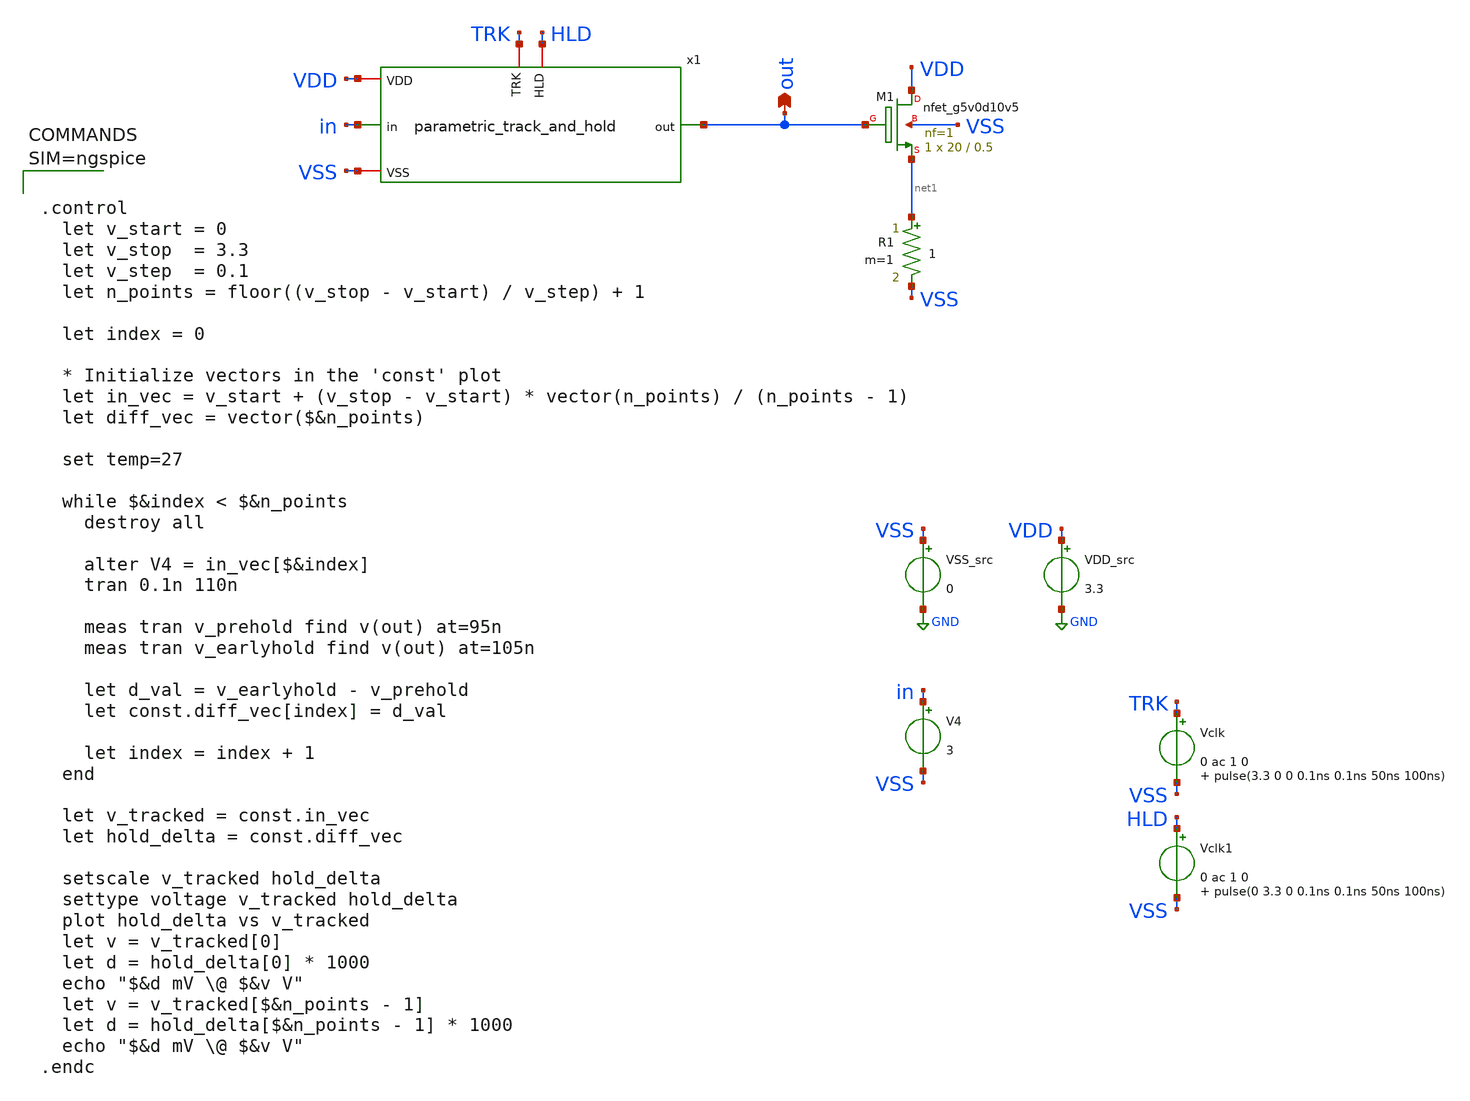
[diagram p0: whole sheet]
** sch_path: xschem/hold_testbench.sch
**.subckt hold_testbench out
*.opin out
VDD_src VDD GND 3.3
VSS_src VSS GND 0
V4 in VSS 3
XM1 VDD out net1 VSS sky130_fd_pr__nfet_g5v0d10v5 L=0.5 W=20 nf=1 ad='int((nf+1)/2) * W/nf * 0.29' as='int((nf+2)/2) * W/nf * 0.29'
+ pd='2*int((nf+1)/2) * (W/nf + 0.29)' ps='2*int((nf+2)/2) * (W/nf + 0.29)' nrd='0.29 / W' nrs='0.29 / W'
+ sa=0 sb=0 sd=0 mult=1 m=1
R1 net1 VSS 1 m=1
Vclk TRK VSS 0 ac 1 0 pulse(3.3 0 0 0.1ns 0.1ns 50ns 100ns)
Vclk1 HLD VSS 0 ac 1 0 pulse(0 3.3 0 0.1ns 0.1ns 50ns 100ns)
x1 HLD TRK VDD VSS out in parametric_track_and_hold WT=1 PFT=1.21 PF=2 WS=5 WB=5 CB=18
**** begin user architecture code

** opencircuitdesign pdks install
.lib $::SKYWATER_MODELS/sky130.lib.spice ss





.control
  let v_start = 0
  let v_stop  = 3.3
  let v_step  = 0.1
  let n_points = floor((v_stop - v_start) / v_step) + 1

  let index = 0

  * Initialize vectors in the 'const' plot
  let in_vec = v_start + (v_stop - v_start) * vector(n_points) / (n_points - 1)
  let diff_vec = vector($&n_points)

  set temp=27

  while $&index < $&n_points
    destroy all

    alter V4 = in_vec[$&index]
    tran 0.1n 110n

    meas tran v_prehold find v(out) at=95n
    meas tran v_earlyhold find v(out) at=105n

    let d_val = v_earlyhold - v_prehold
    let const.diff_vec[index] = d_val

    let index = index + 1
  end

  let v_tracked = const.in_vec
  let hold_delta = const.diff_vec

  setscale v_tracked hold_delta
  settype voltage v_tracked hold_delta
  plot hold_delta vs v_tracked
  let v = v_tracked[0]
  let d = hold_delta[0] * 1000
  echo "$&d mV \@ $&v V"
  let v = v_tracked[$&n_points - 1]
  let d = hold_delta[$&n_points - 1] * 1000
  echo "$&d mV \@ $&v V"
.endc



**** end user architecture code
**.ends

* expanding   symbol:  parametric_track_and_hold.sym # of pins=6
** sym_path: xschem/parametric_track_and_hold.sym
** sch_path: xschem/parametric_track_and_hold.sch
.subckt parametric_track_and_hold HLD TRK VDD VSS out in  WT=1 PFT=1.21 PF=2 WS=5 WB=5 CB=18
*.iopin VSS
*.iopin VDD
*.ipin in
*.opin out
*.iopin TRK
*.iopin HLD
XC1 out VSS sky130_fd_pr__cap_mim_m3_1 W=5 L=5 MF=1 m=1
XM1 out X in VSS sky130_fd_pr__nfet_g5v0d10v5 L=0.5 W={WT} nf=1 ad='int((nf+1)/2) * W/nf * 0.29' as='int((nf+2)/2) * W/nf * 0.29'
+ pd='2*int((nf+1)/2) * (W/nf + 0.29)' ps='2*int((nf+2)/2) * (W/nf + 0.29)' nrd='0.29 / W' nrs='0.29 / W'
+ sa=0 sb=0 sd=0 mult=1 m=1
XM1p out net1 in VDD sky130_fd_pr__pfet_g5v0d10v5 L=0.5 W={WT*PFT} nf=1 ad='int((nf+1)/2) * W/nf * 0.29'
+ as='int((nf+2)/2) * W/nf * 0.29' pd='2*int((nf+1)/2) * (W/nf + 0.29)' ps='2*int((nf+2)/2) * (W/nf + 0.29)'
+ nrd='0.29 / W' nrs='0.29 / W' sa=0 sb=0 sd=0 mult=1 m=1
XM4 VSS HLD X VSS sky130_fd_pr__nfet_g5v0d10v5 L=0.5 W={WS} nf=1 ad='int((nf+1)/2) * W/nf * 0.29' as='int((nf+2)/2) * W/nf * 0.29'
+ pd='2*int((nf+1)/2) * (W/nf + 0.29)' ps='2*int((nf+2)/2) * (W/nf + 0.29)' nrd='0.29 / W' nrs='0.29 / W'
+ sa=0 sb=0 sd=0 mult=1 m=1
XM4p net1 TRK VDD VDD sky130_fd_pr__pfet_g5v0d10v5 L=0.5 W={WS*PF} nf=1 ad='int((nf+1)/2) * W/nf * 0.29'
+ as='int((nf+2)/2) * W/nf * 0.29' pd='2*int((nf+1)/2) * (W/nf + 0.29)' ps='2*int((nf+2)/2) * (W/nf + 0.29)'
+ nrd='0.29 / W' nrs='0.29 / W' sa=0 sb=0 sd=0 mult=1 m=1
XM2 X HLD P P sky130_fd_pr__pfet_g5v0d10v5 L=0.5 W={WS*PF} nf=1 ad='int((nf+1)/2) * W/nf * 0.29' as='int((nf+2)/2) * W/nf * 0.29'
+ pd='2*int((nf+1)/2) * (W/nf + 0.29)' ps='2*int((nf+2)/2) * (W/nf + 0.29)' nrd='0.29 / W' nrs='0.29 / W'
+ sa=0 sb=0 sd=0 mult=1 m=1
XM2p net2 TRK net1 net2 sky130_fd_pr__nfet_g5v0d10v5 L=0.5 W={WS} nf=1 ad='int((nf+1)/2) * W/nf * 0.29'
+ as='int((nf+2)/2) * W/nf * 0.29' pd='2*int((nf+1)/2) * (W/nf + 0.29)' ps='2*int((nf+2)/2) * (W/nf + 0.29)'
+ nrd='0.29 / W' nrs='0.29 / W' sa=0 sb=0 sd=0 mult=1 m=1
XM3 in X Q VSS sky130_fd_pr__nfet_g5v0d10v5 L=0.5 W={WB} nf=1 ad='int((nf+1)/2) * W/nf * 0.29' as='int((nf+2)/2) * W/nf * 0.29'
+ pd='2*int((nf+1)/2) * (W/nf + 0.29)' ps='2*int((nf+2)/2) * (W/nf + 0.29)' nrd='0.29 / W' nrs='0.29 / W'
+ sa=0 sb=0 sd=0 mult=1 m=1
XM6 Q HLD VSS VSS sky130_fd_pr__nfet_g5v0d10v5 L=0.5 W={WB} nf=1 ad='int((nf+1)/2) * W/nf * 0.29' as='int((nf+2)/2) * W/nf * 0.29'
+ pd='2*int((nf+1)/2) * (W/nf + 0.29)' ps='2*int((nf+2)/2) * (W/nf + 0.29)' nrd='0.29 / W' nrs='0.29 / W'
+ sa=0 sb=0 sd=0 mult=1 m=1
XM3p net3 net1 in VDD sky130_fd_pr__pfet_g5v0d10v5 L=0.5 W={WB*PF} nf=1 ad='int((nf+1)/2) * W/nf * 0.29'
+ as='int((nf+2)/2) * W/nf * 0.29' pd='2*int((nf+1)/2) * (W/nf + 0.29)' ps='2*int((nf+2)/2) * (W/nf + 0.29)'
+ nrd='0.29 / W' nrs='0.29 / W' sa=0 sb=0 sd=0 mult=1 m=1
XM6p VDD TRK net3 VDD sky130_fd_pr__pfet_g5v0d10v5 L=0.5 W={WB*PF} nf=1 ad='int((nf+1)/2) * W/nf * 0.29'
+ as='int((nf+2)/2) * W/nf * 0.29' pd='2*int((nf+1)/2) * (W/nf + 0.29)' ps='2*int((nf+2)/2) * (W/nf + 0.29)'
+ nrd='0.29 / W' nrs='0.29 / W' sa=0 sb=0 sd=0 mult=1 m=1
XM5 P X VDD P sky130_fd_pr__pfet_g5v0d10v5 L=0.5 W={WB*PF} nf=1 ad='int((nf+1)/2) * W/nf * 0.29' as='int((nf+2)/2) * W/nf * 0.29'
+ pd='2*int((nf+1)/2) * (W/nf + 0.29)' ps='2*int((nf+2)/2) * (W/nf + 0.29)' nrd='0.29 / W' nrs='0.29 / W'
+ sa=0 sb=0 sd=0 mult=1 m=1
XCb P Q sky130_fd_pr__cap_mim_m3_1 W={CB} L={CB} MF=1 m=1
XCbp net2 net3 sky130_fd_pr__cap_mim_m3_1 W={CB} L={CB} MF=1 m=1
XM5p VSS net1 net2 net2 sky130_fd_pr__nfet_g5v0d10v5 L=0.5 W={WB*PF} nf=1 ad='int((nf+1)/2) * W/nf * 0.29'
+ as='int((nf+2)/2) * W/nf * 0.29' pd='2*int((nf+1)/2) * (W/nf + 0.29)' ps='2*int((nf+2)/2) * (W/nf + 0.29)'
+ nrd='0.29 / W' nrs='0.29 / W' sa=0 sb=0 sd=0 mult=1 m=1
.ends

.GLOBAL GND
.end
